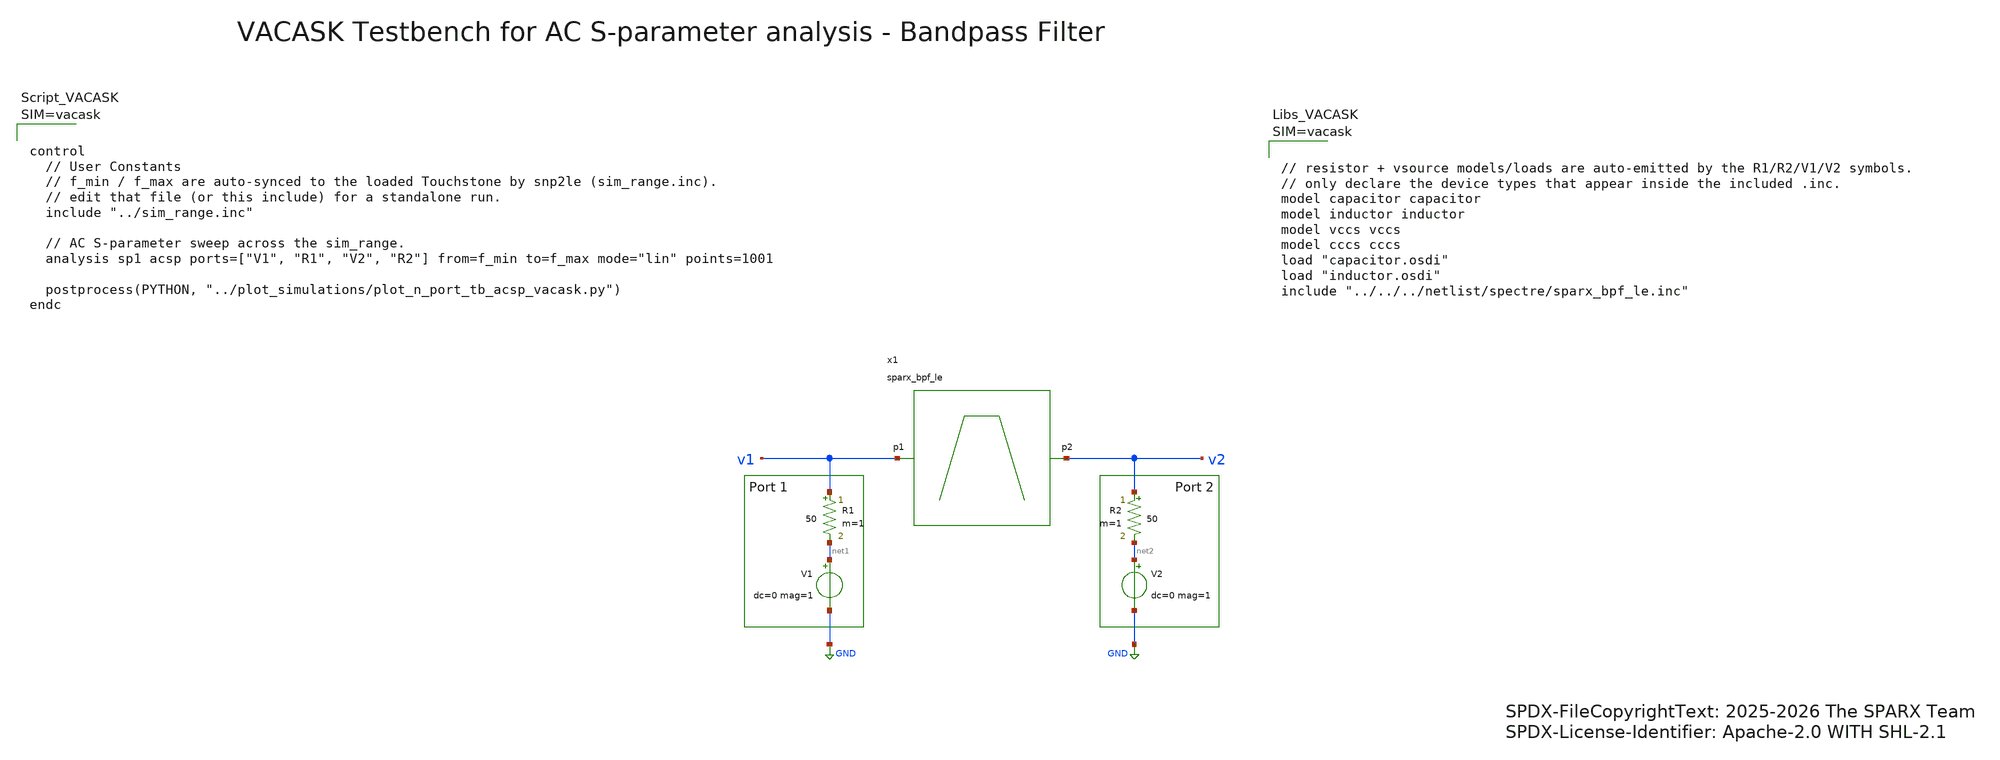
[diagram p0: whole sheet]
** sch_path: testbenches/xschem/sparx_bpf_le_tb_acsp_vacask.sch
* SPDX-FileCopyrightText: 2025-2026 The SPARX Team
* SPDX-License-Identifier: Apache-2.0 WITH SHL-2.1
**.subckt sparx_bpf_le_tb_acsp_vacask
R1 v1 net1 50 m=1
V1 net1 GND dc=0 mag=1
R2 v2 net2 50 m=1
V2 net2 GND dc=0 mag=1
x1 v1 v2 sparx_bpf_le
**** begin user architecture code






**** end user architecture code
**.ends
.GLOBAL GND
.end
